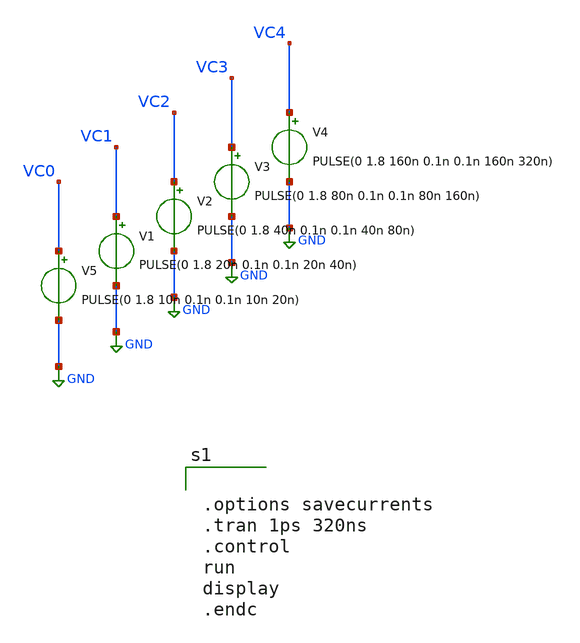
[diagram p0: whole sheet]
** sch_path: xschem/source_binary_cnt_test.sch
**.subckt source_binary_cnt_test
V5 VC0 GND PULSE(0 1.8 10n 0.1n 0.1n 10n 20n)
V1 VC1 GND PULSE(0 1.8 20n 0.1n 0.1n 20n 40n)
V2 VC2 GND PULSE(0 1.8 40n 0.1n 0.1n 40n 80n)
V3 VC3 GND PULSE(0 1.8 80n 0.1n 0.1n 80n 160n)
V4 VC4 GND PULSE(0 1.8 160n 0.1n 0.1n 160n 320n)
**** begin user architecture code


.options savecurrents
.tran 1ps 320ns
.control
run
display
.endc

**** end user architecture code
**.ends
.GLOBAL GND
.end
